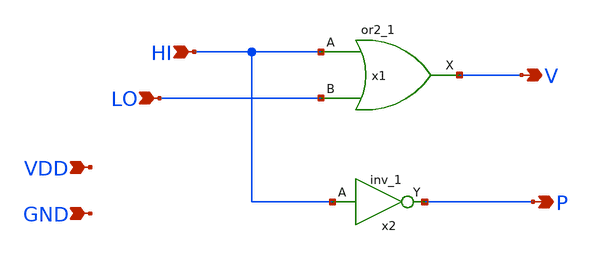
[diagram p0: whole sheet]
** sch_path: frontend/xschem/lzc2.sch
**.subckt lzc2 HI LO V P VDD GND
*.ipin HI
*.ipin LO
*.opin V
*.opin P
*.ipin VDD
*.ipin GND
x1 HI LO GND GND VDD VDD V sky130_fd_sc_hd__or2_1
x2 HI GND GND VDD VDD P sky130_fd_sc_hd__inv_1
**.ends
.end
